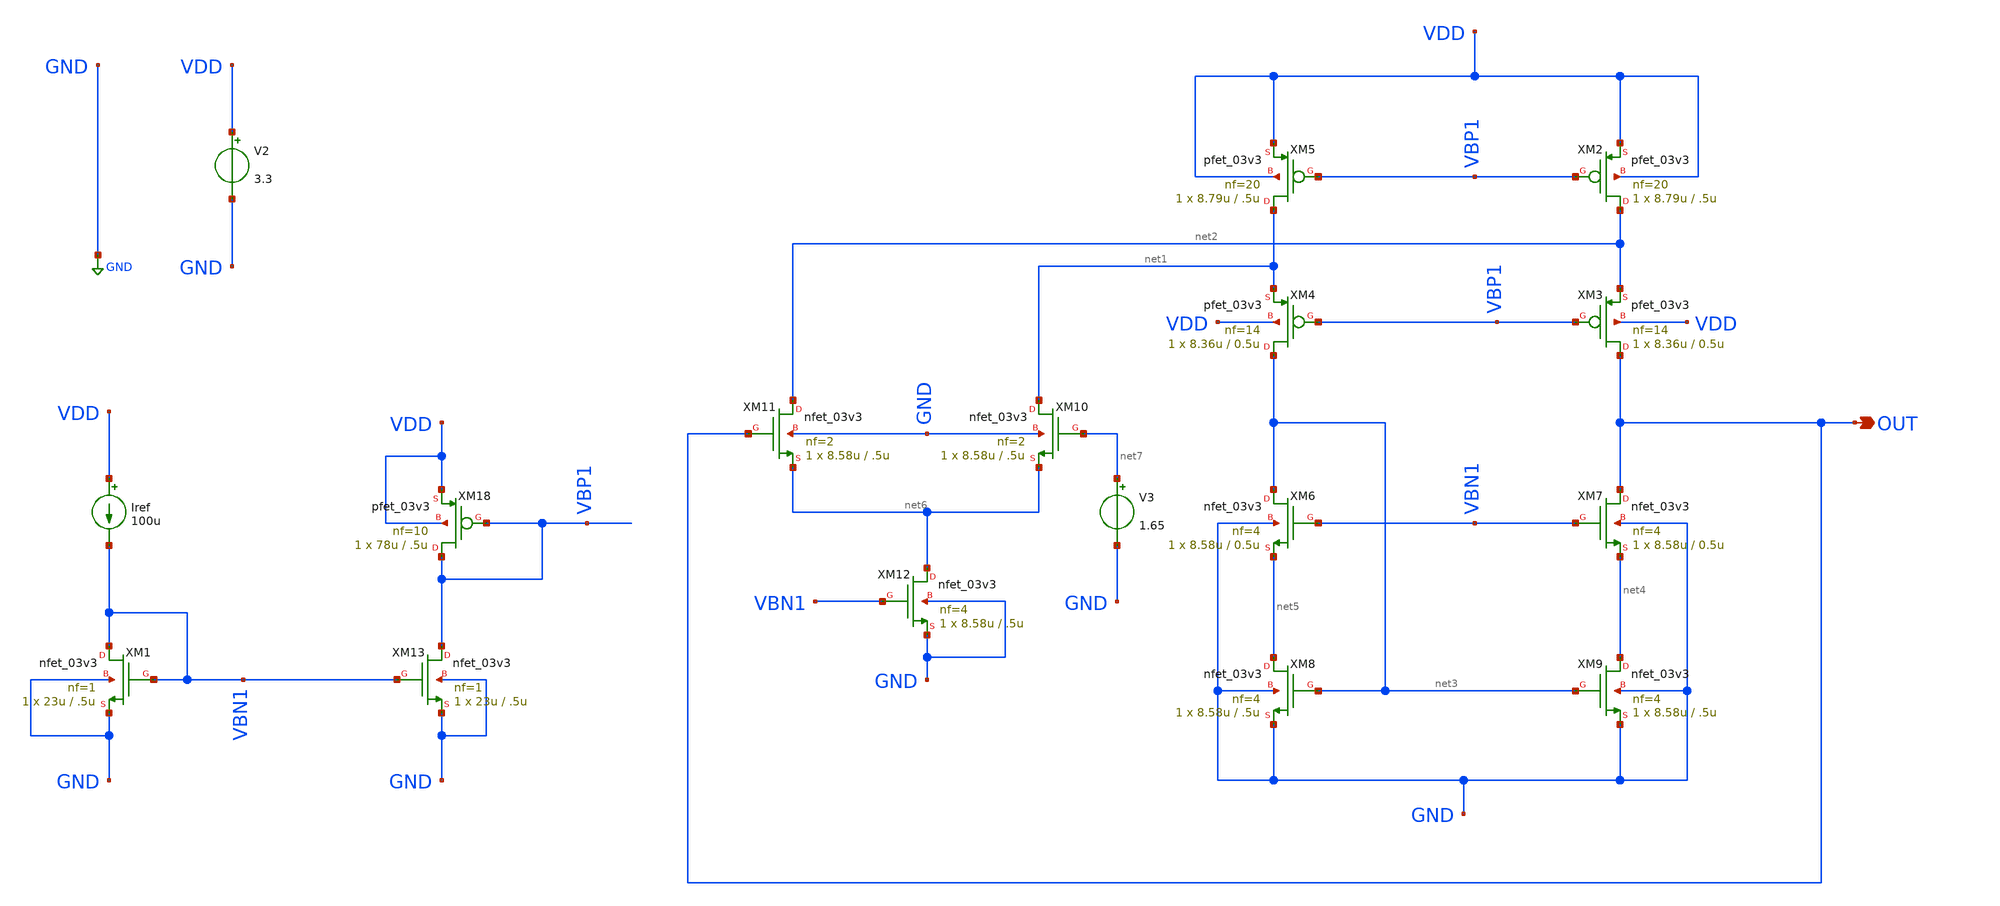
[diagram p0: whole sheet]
** sch_path: designs/libs/core_amps/ota_folded_cascode/folded_tb_schem.sch
**.subckt folded_tb_schem OUT
*.opin OUT
Iref VDD VBN1 100u
V2 VDD GND 3.3
XM1 VBN1 VBN1 GND GND nfet_03v3 L=.5u W=23u nf=1 ad='int((nf+1)/2) * W/nf * 0.18u' as='int((nf+2)/2) * W/nf * 0.18u'
+ pd='2*int((nf+1)/2) * (W/nf + 0.18u)' ps='2*int((nf+2)/2) * (W/nf + 0.18u)' nrd='0.18u / W' nrs='0.18u / W'
+ sa=0 sb=0 sd=0 m=1
XM2 net2 VBP1 VDD VDD pfet_03v3 L=.5u W=8.79u nf=20 ad='int((nf+1)/2) * W/nf * 0.18u' as='int((nf+2)/2) * W/nf * 0.18u'
+ pd='2*int((nf+1)/2) * (W/nf + 0.18u)' ps='2*int((nf+2)/2) * (W/nf + 0.18u)' nrd='0.18u / W' nrs='0.18u / W'
+ sa=0 sb=0 sd=0 m=1
XM3 OUT VBP1 net2 VDD pfet_03v3 L=0.5u W=8.36u nf=14 ad='int((nf+1)/2) * W/nf * 0.18u' as='int((nf+2)/2) * W/nf * 0.18u'
+ pd='2*int((nf+1)/2) * (W/nf + 0.18u)' ps='2*int((nf+2)/2) * (W/nf + 0.18u)' nrd='0.18u / W' nrs='0.18u / W'
+ sa=0 sb=0 sd=0 m=1
XM4 net3 VBP1 net1 VDD pfet_03v3 L=0.5u W=8.36u nf=14 ad='int((nf+1)/2) * W/nf * 0.18u' as='int((nf+2)/2) * W/nf * 0.18u'
+ pd='2*int((nf+1)/2) * (W/nf + 0.18u)' ps='2*int((nf+2)/2) * (W/nf + 0.18u)' nrd='0.18u / W' nrs='0.18u / W'
+ sa=0 sb=0 sd=0 m=1
XM5 net1 VBP1 VDD VDD pfet_03v3 L=.5u W=8.79u nf=20 ad='int((nf+1)/2) * W/nf * 0.18u' as='int((nf+2)/2) * W/nf * 0.18u'
+ pd='2*int((nf+1)/2) * (W/nf + 0.18u)' ps='2*int((nf+2)/2) * (W/nf + 0.18u)' nrd='0.18u / W' nrs='0.18u / W'
+ sa=0 sb=0 sd=0 m=1
XM6 net3 VBN1 net5 GND nfet_03v3 L=0.5u W=8.58u nf=4 ad='int((nf+1)/2) * W/nf * 0.18u' as='int((nf+2)/2) * W/nf * 0.18u'
+ pd='2*int((nf+1)/2) * (W/nf + 0.18u)' ps='2*int((nf+2)/2) * (W/nf + 0.18u)' nrd='0.18u / W' nrs='0.18u / W'
+ sa=0 sb=0 sd=0 m=1
XM7 OUT VBN1 net4 GND nfet_03v3 L=0.5u W=8.58u nf=4 ad='int((nf+1)/2) * W/nf * 0.18u' as='int((nf+2)/2) * W/nf * 0.18u'
+ pd='2*int((nf+1)/2) * (W/nf + 0.18u)' ps='2*int((nf+2)/2) * (W/nf + 0.18u)' nrd='0.18u / W' nrs='0.18u / W'
+ sa=0 sb=0 sd=0 m=1
XM8 net5 net3 GND GND nfet_03v3 L=.5u W=8.58u nf=4 ad='int((nf+1)/2) * W/nf * 0.18u' as='int((nf+2)/2) * W/nf * 0.18u'
+ pd='2*int((nf+1)/2) * (W/nf + 0.18u)' ps='2*int((nf+2)/2) * (W/nf + 0.18u)' nrd='0.18u / W' nrs='0.18u / W'
+ sa=0 sb=0 sd=0 m=1
XM9 net4 net3 GND GND nfet_03v3 L=.5u W=8.58u nf=4 ad='int((nf+1)/2) * W/nf * 0.18u' as='int((nf+2)/2) * W/nf * 0.18u'
+ pd='2*int((nf+1)/2) * (W/nf + 0.18u)' ps='2*int((nf+2)/2) * (W/nf + 0.18u)' nrd='0.18u / W' nrs='0.18u / W'
+ sa=0 sb=0 sd=0 m=1
XM10 net1 net7 net6 GND nfet_03v3 L=.5u W=8.58u nf=2 ad='int((nf+1)/2) * W/nf * 0.18u' as='int((nf+2)/2) * W/nf * 0.18u'
+ pd='2*int((nf+1)/2) * (W/nf + 0.18u)' ps='2*int((nf+2)/2) * (W/nf + 0.18u)' nrd='0.18u / W' nrs='0.18u / W'
+ sa=0 sb=0 sd=0 m=1
XM12 net6 VBN1 GND GND nfet_03v3 L=.5u W=8.58u nf=4 ad='int((nf+1)/2) * W/nf * 0.18u' as='int((nf+2)/2) * W/nf * 0.18u'
+ pd='2*int((nf+1)/2) * (W/nf + 0.18u)' ps='2*int((nf+2)/2) * (W/nf + 0.18u)' nrd='0.18u / W' nrs='0.18u / W'
+ sa=0 sb=0 sd=0 m=1
XM18 VBP1 VBP1 VDD VDD pfet_03v3 L=.5u W=78u nf=10 ad='int((nf+1)/2) * W/nf * 0.18u' as='int((nf+2)/2) * W/nf * 0.18u'
+ pd='2*int((nf+1)/2) * (W/nf + 0.18u)' ps='2*int((nf+2)/2) * (W/nf + 0.18u)' nrd='0.18u / W' nrs='0.18u / W'
+ sa=0 sb=0 sd=0 m=1
XM11 net2 OUT net6 GND nfet_03v3 L=.5u W=8.58u nf=2 ad='int((nf+1)/2) * W/nf * 0.18u' as='int((nf+2)/2) * W/nf * 0.18u'
+ pd='2*int((nf+1)/2) * (W/nf + 0.18u)' ps='2*int((nf+2)/2) * (W/nf + 0.18u)' nrd='0.18u / W' nrs='0.18u / W'
+ sa=0 sb=0 sd=0 m=1
V3 net7 GND 1.65
XM13 VBP1 VBN1 GND GND nfet_03v3 L=.5u W=23u nf=1 ad='int((nf+1)/2) * W/nf * 0.18u' as='int((nf+2)/2) * W/nf * 0.18u'
+ pd='2*int((nf+1)/2) * (W/nf + 0.18u)' ps='2*int((nf+2)/2) * (W/nf + 0.18u)' nrd='0.18u / W' nrs='0.18u / W'
+ sa=0 sb=0 sd=0 m=1
**** begin user architecture code

.include $::180MCU_MODELS/design.ngspice
.lib $::180MCU_MODELS/sm141064.ngspice typical



.control
op

* --- key bias nodes (should be ~mid-supply / sane VGS) ---
print v(OUT) v(VBN1) v(VBP1)

* --- reference current: should be ~100u through the diode NMOS XM1 ---
print @m.xm1.m0[id]

* --- gm/id on every device (target ~10) ---
let gmid_m1  = @m.xm1.m0[gm]/@m.xm1.m0[id]
let gmid_m2  = @m.xm2.m0[gm]/@m.xm2.m0[id]
let gmid_m3  = @m.xm3.m0[gm]/@m.xm3.m0[id]
let gmid_m4  = @m.xm4.m0[gm]/@m.xm4.m0[id]
let gmid_m5  = @m.xm5.m0[gm]/@m.xm5.m0[id]
let gmid_m6  = @m.xm6.m0[gm]/@m.xm6.m0[id]
let gmid_m7  = @m.xm7.m0[gm]/@m.xm7.m0[id]
let gmid_m8  = @m.xm8.m0[gm]/@m.xm8.m0[id]
let gmid_m9  = @m.xm9.m0[gm]/@m.xm9.m0[id]
let gmid_m10 = @m.xm10.m0[gm]/@m.xm10.m0[id]
let gmid_m11 = @m.xm11.m0[gm]/@m.xm11.m0[id]
let gmid_m12 = @m.xm12.m0[gm]/@m.xm12.m0[id]
let gmid_m13 = @m.xm13.m0[gm]/@m.xm13.m0[id]
let gmid_m18 = @m.xm18.m0[gm]/@m.xm18.m0[id]
print gmid_m1 gmid_m2 gmid_m3 gmid_m4 gmid_m5
print gmid_m6 gmid_m7 gmid_m8 gmid_m9 gmid_m10
print gmid_m11 gmid_m12 gmid_m13 gmid_m18

print @m.xm1.m0[id]  @m.xm2.m0[id]  @m.xm3.m0[id]
print @m.xm4.m0[id]  @m.xm5.m0[id]  @m.xm6.m0[id]
print @m.xm7.m0[id]  @m.xm8.m0[id]  @m.xm9.m0[id]
print @m.xm10.m0[id] @m.xm11.m0[id] @m.xm12.m0[id]
print @m.xm13.m0[id] @m.xm18.m0[id]

print @m.xm18.m0[vgs] @m.xm18.m0[id]    $ PMOS reference
print @m.xm2.m0[vgs]  @m.xm2.m0[id]     $ PMOS mirror that's wrong
print @m.xm1.m0[vgs]  @m.xm1.m0[id]     $ NMOS reference
print @m.xm6.m0[vgs]  @m.xm6.m0[id]     $ NMOS mirror that's wrong

.endc


**** end user architecture code
**.ends
.GLOBAL GND
.end
